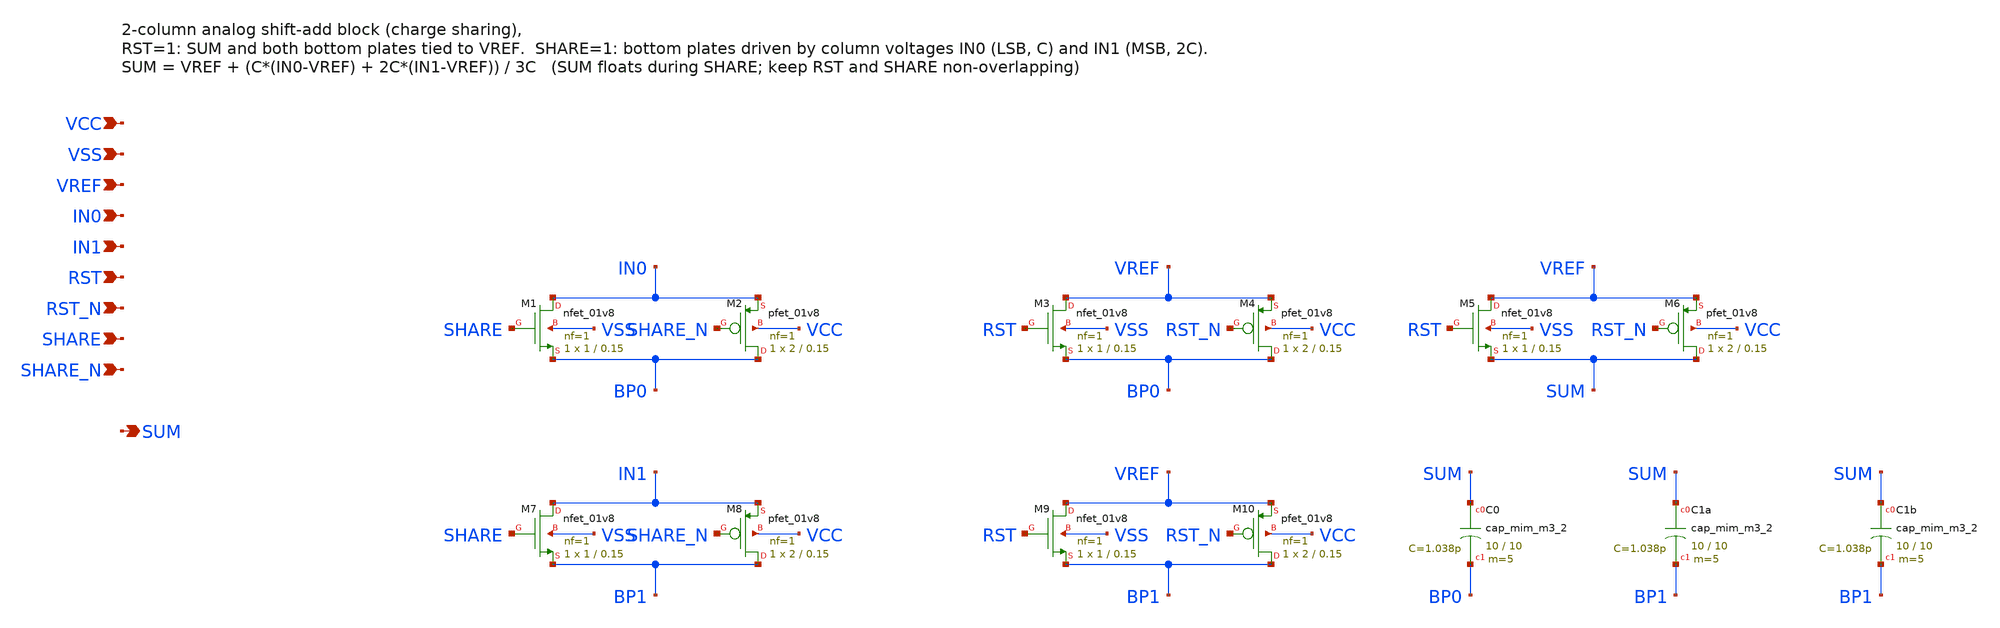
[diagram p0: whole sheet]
** sch_path: CiM components/shift_add_2col.sch
**.subckt shift_add_2col VCC VSS VREF IN0 IN1 RST RST_N SHARE SHARE_N SUM
*.ipin VCC
*.ipin VSS
*.ipin VREF
*.ipin IN0
*.ipin IN1
*.ipin RST
*.ipin RST_N
*.ipin SHARE
*.ipin SHARE_N
*.opin SUM
XM1 IN0 SHARE BP0 VSS sky130_fd_pr__nfet_01v8 L=0.15 W=1 nf=1 ad='int((nf+1)/2) * W/nf * 0.29' as='int((nf+2)/2) * W/nf * 0.29'
+ pd='2*int((nf+1)/2) * (W/nf + 0.29)' ps='2*int((nf+2)/2) * (W/nf + 0.29)' nrd='0.29 / W' nrs='0.29 / W'
+ sa=0 sb=0 sd=0 mult=1 m=1
XM2 BP0 SHARE_N IN0 VCC sky130_fd_pr__pfet_01v8 L=0.15 W=2 nf=1 ad='int((nf+1)/2) * W/nf * 0.29' as='int((nf+2)/2) * W/nf * 0.29'
+ pd='2*int((nf+1)/2) * (W/nf + 0.29)' ps='2*int((nf+2)/2) * (W/nf + 0.29)' nrd='0.29 / W' nrs='0.29 / W'
+ sa=0 sb=0 sd=0 mult=1 m=1
XM3 VREF RST BP0 VSS sky130_fd_pr__nfet_01v8 L=0.15 W=1 nf=1 ad='int((nf+1)/2) * W/nf * 0.29' as='int((nf+2)/2) * W/nf * 0.29'
+ pd='2*int((nf+1)/2) * (W/nf + 0.29)' ps='2*int((nf+2)/2) * (W/nf + 0.29)' nrd='0.29 / W' nrs='0.29 / W'
+ sa=0 sb=0 sd=0 mult=1 m=1
XM4 BP0 RST_N VREF VCC sky130_fd_pr__pfet_01v8 L=0.15 W=2 nf=1 ad='int((nf+1)/2) * W/nf * 0.29' as='int((nf+2)/2) * W/nf * 0.29'
+ pd='2*int((nf+1)/2) * (W/nf + 0.29)' ps='2*int((nf+2)/2) * (W/nf + 0.29)' nrd='0.29 / W' nrs='0.29 / W'
+ sa=0 sb=0 sd=0 mult=1 m=1
XM5 VREF RST SUM VSS sky130_fd_pr__nfet_01v8 L=0.15 W=1 nf=1 ad='int((nf+1)/2) * W/nf * 0.29' as='int((nf+2)/2) * W/nf * 0.29'
+ pd='2*int((nf+1)/2) * (W/nf + 0.29)' ps='2*int((nf+2)/2) * (W/nf + 0.29)' nrd='0.29 / W' nrs='0.29 / W'
+ sa=0 sb=0 sd=0 mult=1 m=1
XM6 SUM RST_N VREF VCC sky130_fd_pr__pfet_01v8 L=0.15 W=2 nf=1 ad='int((nf+1)/2) * W/nf * 0.29' as='int((nf+2)/2) * W/nf * 0.29'
+ pd='2*int((nf+1)/2) * (W/nf + 0.29)' ps='2*int((nf+2)/2) * (W/nf + 0.29)' nrd='0.29 / W' nrs='0.29 / W'
+ sa=0 sb=0 sd=0 mult=1 m=1
XM7 IN1 SHARE BP1 VSS sky130_fd_pr__nfet_01v8 L=0.15 W=1 nf=1 ad='int((nf+1)/2) * W/nf * 0.29' as='int((nf+2)/2) * W/nf * 0.29'
+ pd='2*int((nf+1)/2) * (W/nf + 0.29)' ps='2*int((nf+2)/2) * (W/nf + 0.29)' nrd='0.29 / W' nrs='0.29 / W'
+ sa=0 sb=0 sd=0 mult=1 m=1
XM8 BP1 SHARE_N IN1 VCC sky130_fd_pr__pfet_01v8 L=0.15 W=2 nf=1 ad='int((nf+1)/2) * W/nf * 0.29' as='int((nf+2)/2) * W/nf * 0.29'
+ pd='2*int((nf+1)/2) * (W/nf + 0.29)' ps='2*int((nf+2)/2) * (W/nf + 0.29)' nrd='0.29 / W' nrs='0.29 / W'
+ sa=0 sb=0 sd=0 mult=1 m=1
XM9 VREF RST BP1 VSS sky130_fd_pr__nfet_01v8 L=0.15 W=1 nf=1 ad='int((nf+1)/2) * W/nf * 0.29' as='int((nf+2)/2) * W/nf * 0.29'
+ pd='2*int((nf+1)/2) * (W/nf + 0.29)' ps='2*int((nf+2)/2) * (W/nf + 0.29)' nrd='0.29 / W' nrs='0.29 / W'
+ sa=0 sb=0 sd=0 mult=1 m=1
XM10 BP1 RST_N VREF VCC sky130_fd_pr__pfet_01v8 L=0.15 W=2 nf=1 ad='int((nf+1)/2) * W/nf * 0.29' as='int((nf+2)/2) * W/nf * 0.29'
+ pd='2*int((nf+1)/2) * (W/nf + 0.29)' ps='2*int((nf+2)/2) * (W/nf + 0.29)' nrd='0.29 / W' nrs='0.29 / W'
+ sa=0 sb=0 sd=0 mult=1 m=1
XC0 SUM BP0 sky130_fd_pr__cap_mim_m3_2 W=10 L=10 MF=5 m=5
XC1a SUM BP1 sky130_fd_pr__cap_mim_m3_2 W=10 L=10 MF=5 m=5
XC1b SUM BP1 sky130_fd_pr__cap_mim_m3_2 W=10 L=10 MF=5 m=5
**.ends
.end
